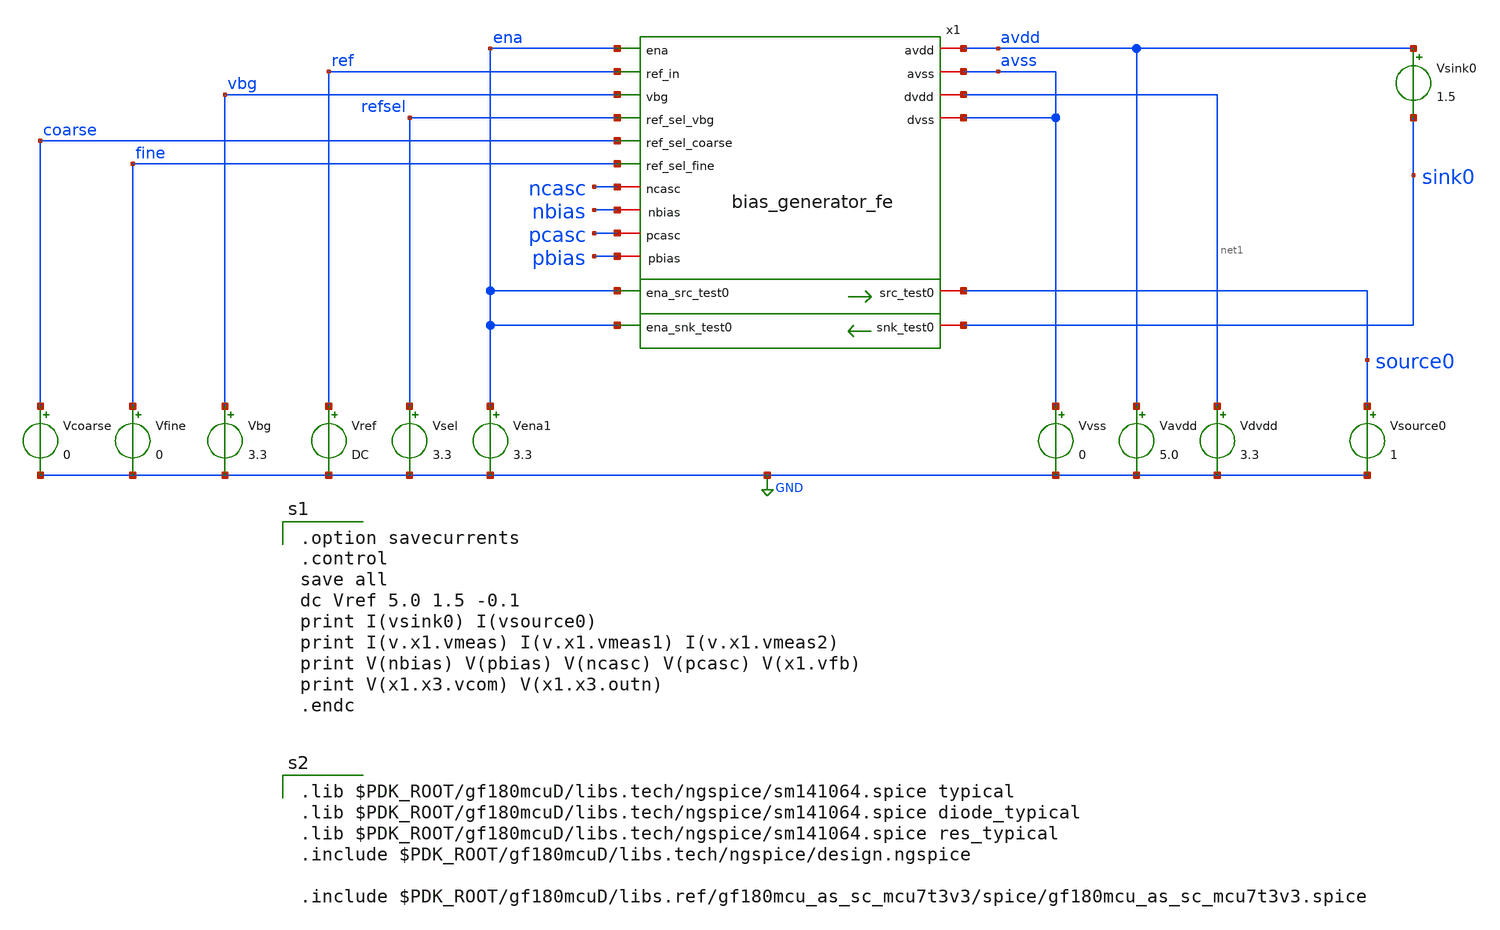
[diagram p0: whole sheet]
** sch_path: projects/programmable_transceiver_platform/analog/core_support/biasgen/xschem/bias_gen_fe_tb.sch
**.subckt bias_gen_fe_tb
Vavdd avdd GND 5.0
Vvss avss GND 0
Vsource0 source0 GND 1
Vsink0 avdd sink0 1.5
Vsel refsel GND 3.3
Vref ref GND DC
Vbg vbg GND 3.3
Vena1 ena GND 3.3
Vdvdd net1 GND 3.3
x1 avdd ena vbg source0 avss net1 ena refsel ref avss nbias pcasc pbias sink0 ena ncasc fine coarse
+ bias_generator_fe
Vfine fine GND 0
Vcoarse coarse GND 0
**** begin user architecture code

.option savecurrents
.control
save all
dc Vref 5.0 1.5 -0.1
print I(vsink0) I(vsource0)
print I(v.x1.vmeas) I(v.x1.vmeas1) I(v.x1.vmeas2)
print V(nbias) V(pbias) V(ncasc) V(pcasc) V(x1.vfb)
print V(x1.x3.vcom) V(x1.x3.outn)
.endc


.lib $PDK_ROOT/gf180mcuD/libs.tech/ngspice/sm141064.spice typical
.lib $PDK_ROOT/gf180mcuD/libs.tech/ngspice/sm141064.spice diode_typical
.lib $PDK_ROOT/gf180mcuD/libs.tech/ngspice/sm141064.spice res_typical
.include $PDK_ROOT/gf180mcuD/libs.tech/ngspice/design.ngspice

.include $PDK_ROOT/gf180mcuD/libs.ref/gf180mcu_as_sc_mcu7t3v3/spice/gf180mcu_as_sc_mcu7t3v3.spice


**** end user architecture code
**.ends
.GLOBAL GND
.end
